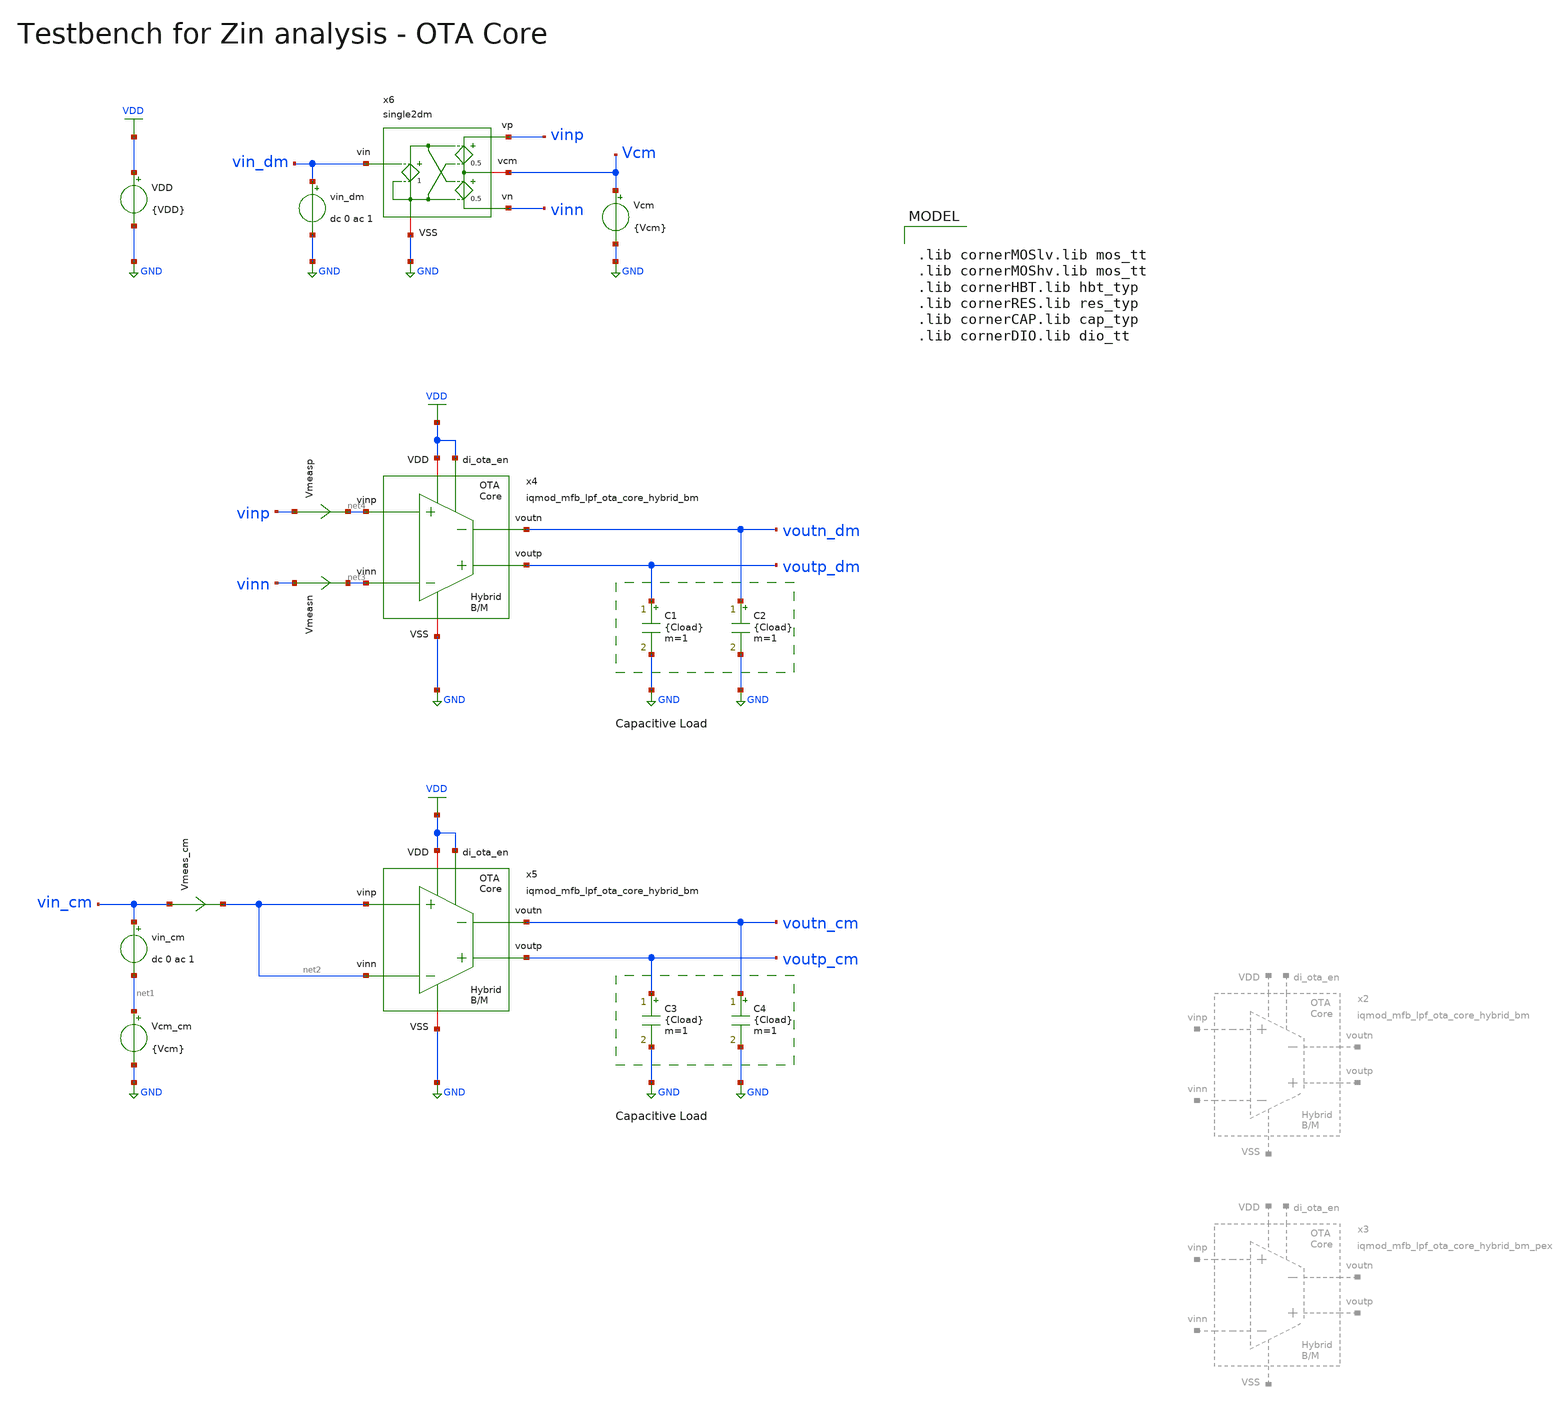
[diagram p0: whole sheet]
** sch_path: ihp130/macros/iqmod/testbenches/iqmod_mfb_lpf_ota_core_tb_Zin.sch
**.subckt iqmod_mfb_lpf_ota_core_tb_Zin
VDD VDD GND {VDD}
C1 voutp_dm GND {Cload} m=1
C2 voutn_dm GND {Cload} m=1
C3 voutp_cm GND {Cload} m=1
C4 voutn_cm GND {Cload} m=1
vin_cm vin_cm net1 dc 0 ac 1
Vmeasp vinp net4 0
.save i(vmeasp)
Vmeasn vinn net3 0
.save i(vmeasn)
Vmeas_cm vin_cm net2 0
.save i(vmeas_cm)
Vcm_cm net1 GND {Vcm}
vin_dm vin_dm GND dc 0 ac 1
x4 voutp_dm voutn_dm net3 net4 VDD GND VDD iqmod_mfb_lpf_ota_core_hybrid_bm
x5 voutp_cm voutn_cm net2 net2 VDD GND VDD iqmod_mfb_lpf_ota_core_hybrid_bm
Vcm Vcm GND {Vcm}
x6 vinp vin_dm Vcm GND vinn single2dm
**** begin user architecture code


.include ../../netlist/pex/iqmod_mfb_lpf_ota_core_hybrid_bm_pex.spice
.param VDD=1.5
.param Vcm=VDD/2
.param temp=27
.param Cload=10p
.options savecurrents klu method=gear reltol=1e-4 abstol=1e-15 gmin=1e-15
.control

* save v(vinp) v(vinn) i(Vmeasp) i(Vmeasn) v(vin_cm) i(Vmeas_cm)
save all

set wr_vecnames
set wr_singlescale

* User Constants
let f_min = 0.1
let f_max = 1G
let fdc = 10

* Operating Point Analysis
op
remzerovec
write iqmod_mfb_lpf_ota_core_tb_Zin.raw
set appendwrite

* AC Analysis
ac dec 101 $&const.f_min $&const.f_max
remzerovec
write iqmod_mfb_lpf_ota_core_tb_Zin.raw

* Plotting Differential Mode Zin
* let Zin_dm = (v(vinp) - v(vinn)) / (i(Vmeasp) - i(Vmeasn))
* let Zin_dm = (v(vinp) - v(vinn)) / (i(Vmeasp) + i(Vmeasn))
let Zin_dm = (v(vinp) - v(vinn)) / i(Vmeasp)
plot Zin_dm ylabel 'DM Zin'

* Plotting Common Mode Zin
let Zin_cm = v(vin_cm) / i(Vmeas_cm)
plot Zin_cm ylabel 'CM Zin'

* Measurements
meas ac Zindc_dm find Zin_dm when frequency = fdc
print Zindc_dm

meas ac Zindc_cm find Zin_cm when frequency = fdc
print Zindc_cm

* Write Data
unset appendwrite
set wr_vecnames
set wr_singlescale
wrdata $PROJECT_PATH/scripts/plot_simulations/data/iqmod_mfb_lpf_ota_core_tb_Zin.txt v(Zin_dm)
+ v(Zin_cm)

*quit
.endc



.lib cornerMOSlv.lib mos_tt
.lib cornerMOShv.lib mos_tt
.lib cornerHBT.lib hbt_typ
.lib cornerRES.lib res_typ
.lib cornerCAP.lib cap_typ
.lib cornerDIO.lib dio_tt

**** end user architecture code
**.ends
.GLOBAL GND
.GLOBAL VDD
.end
